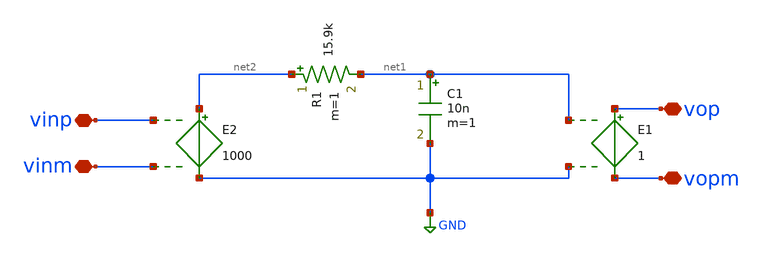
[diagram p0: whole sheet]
** sch_path: work/xschem/buffer.sch
**.subckt buffer vinp vinm vop vopm
*.iopin vinp
*.iopin vinm
*.iopin vop
*.iopin vopm
E1 vop vopm net1 GND 1
E2 net2 GND vinp vinm 1000
R1 net2 net1 15.9k m=1
C1 net1 GND 10n m=1
**.ends
.GLOBAL GND
.end
